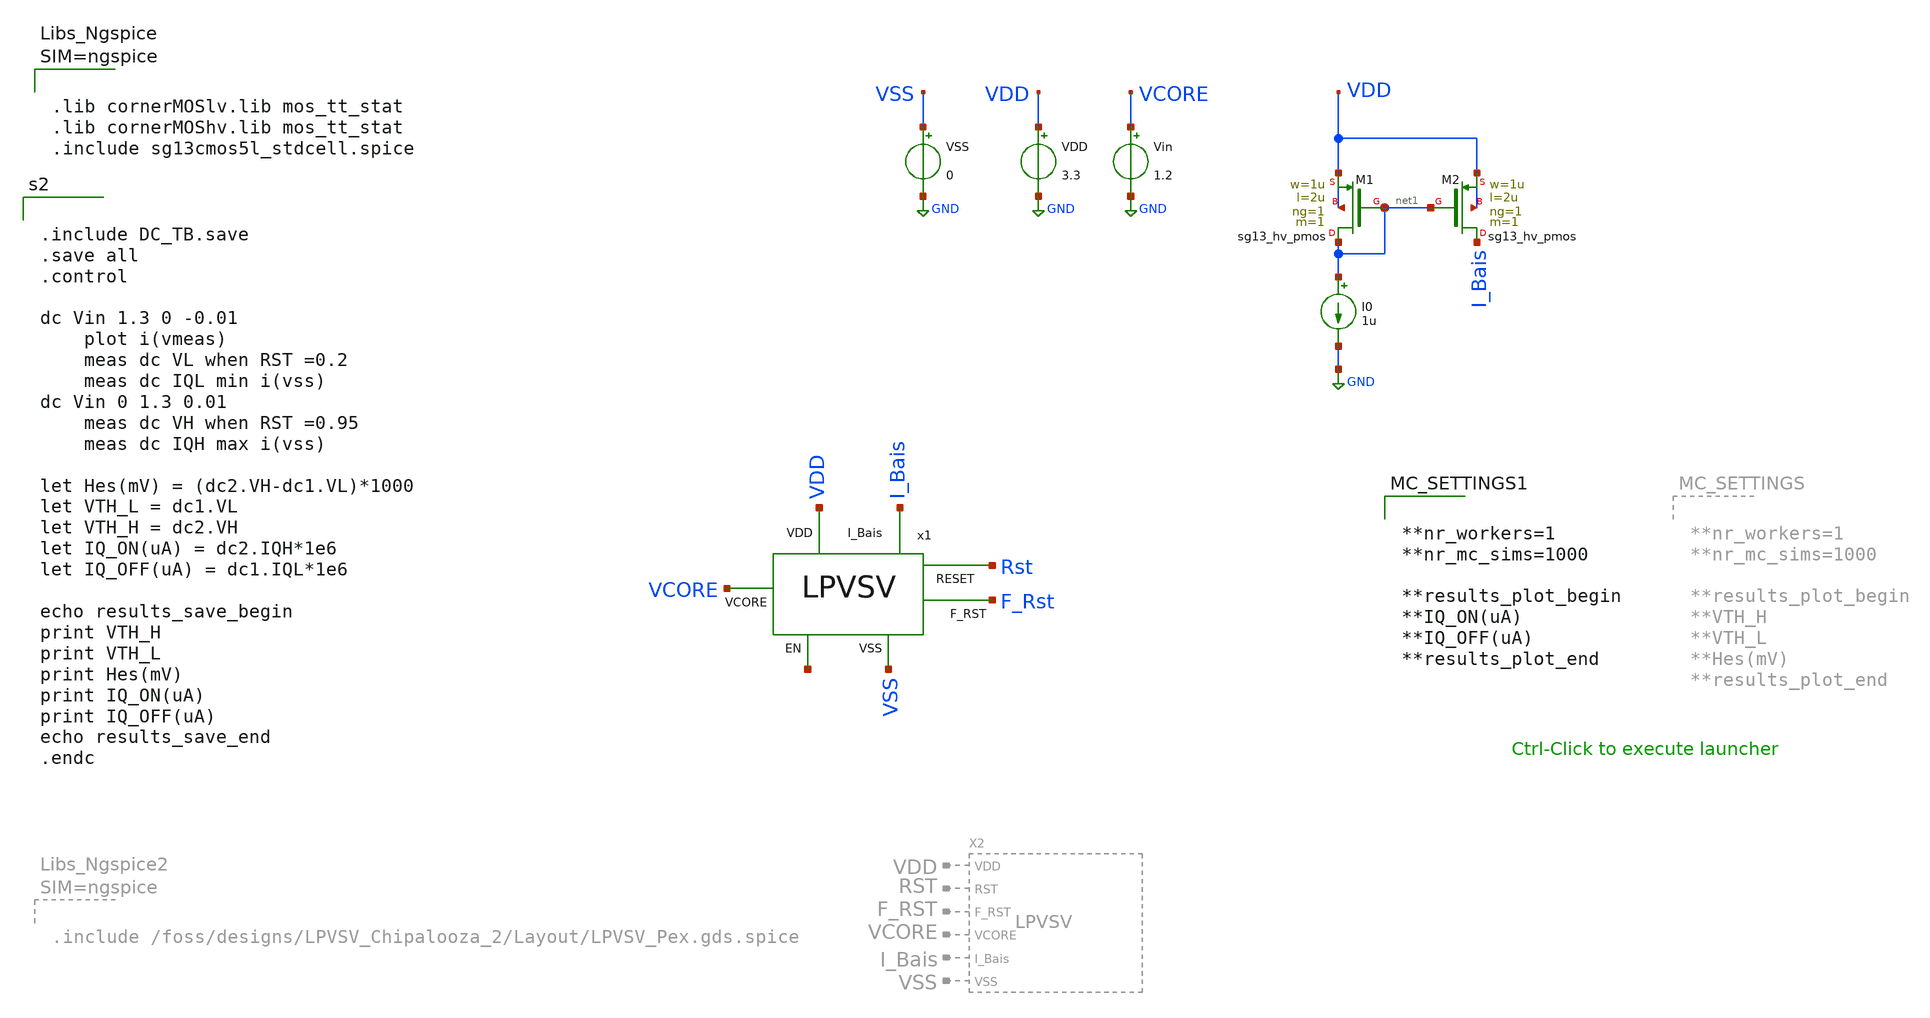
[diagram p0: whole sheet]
** sch_path: Simulation/DC_TB_MC.sch
**.subckt DC_TB_MC
VDD VDD GND 3.3
VSS VSS GND 0
Vin VCORE GND 1.2
x1 VDD VCORE I_Bais Rst F_Rst VSS net2 LPVSV
I0 net1 GND 1u
XM1 net1 net1 VDD VDD sg13_hv_pmos w=1u l=2u ng=1 m=1 mm_ok=1
XM2 I_Bais net1 VDD VDD sg13_hv_pmos w=1u l=2u ng=1 m=1 mm_ok=1
**** begin user architecture code


.include DC_TB.save
.save all
.control

dc Vin 1.3 0 -0.01
	plot i(vmeas)
	meas dc VL when RST =0.2
	meas dc IQL min i(vss)
dc Vin 0 1.3 0.01
	meas dc VH when RST =0.95
	meas dc IQH max i(vss)

let Hes(mV) = (dc2.VH-dc1.VL)*1000
let VTH_L = dc1.VL
let VTH_H = dc2.VH
let IQ_ON(uA) = dc2.IQH*1e6
let IQ_OFF(uA) = dc1.IQL*1e6

echo results_save_begin
print VTH_H
print VTH_L
print Hes(mV)
print IQ_ON(uA)
print IQ_OFF(uA)
echo results_save_end
.endc




.options rshunt = 1e15
.options gmin=1e-9
.options reltol = 0.01 abstol = 1p
.option filetype=ascii





.lib cornerMOSlv.lib mos_tt_stat
.lib cornerMOShv.lib mos_tt_stat
.include sg13cmos5l_stdcell.spice





**nr_workers=1
**nr_mc_sims=1000

**results_plot_begin
**IQ_ON(uA)
**IQ_OFF(uA)
**results_plot_end


**** end user architecture code
**.ends
.GLOBAL GND
.end
